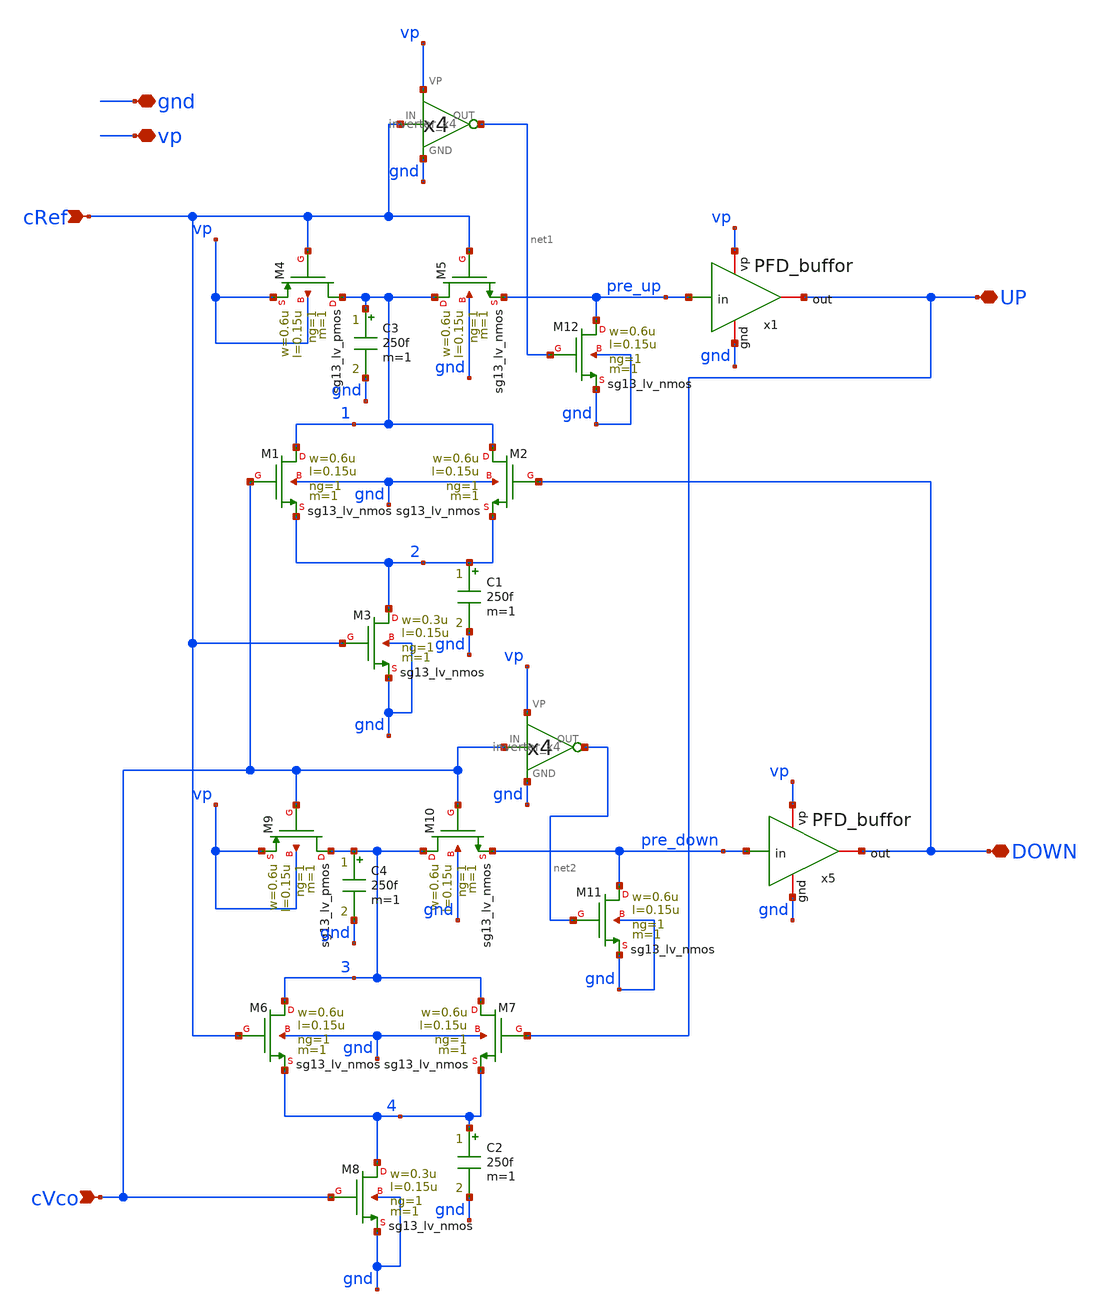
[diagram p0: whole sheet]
** sch_path: PLL0663-main/schematic/xschem/PFD/PFD_cell.sch
**.subckt PFD_cell gnd vp DOWN UP cRef cVco
*.iopin gnd
*.iopin vp
*.iopin DOWN
*.iopin UP
*.ipin cRef
*.ipin cVco
XM1 1 cVco 2 gnd sg13_lv_nmos w=0.6u l=0.15u ng=1 m=1 mm_ok=1
XM2 1 DOWN 2 gnd sg13_lv_nmos w=0.6u l=0.15u ng=1 m=1 mm_ok=1
XM3 2 cRef gnd gnd sg13_lv_nmos w=0.3u l=0.15u ng=1 m=1 mm_ok=1
XM6 3 cRef 4 gnd sg13_lv_nmos w=0.6u l=0.15u ng=1 m=1 mm_ok=1
XM7 3 UP 4 gnd sg13_lv_nmos w=0.6u l=0.15u ng=1 m=1 mm_ok=1
XM8 4 cVco gnd gnd sg13_lv_nmos w=0.3u l=0.15u ng=1 m=1 mm_ok=1
XM4 1 cRef vp vp sg13_lv_pmos w=0.6u l=0.15u ng=1 m=1 mm_ok=1
XM5 1 cRef pre_up gnd sg13_lv_nmos w=0.6u l=0.15u ng=1 m=1 mm_ok=1
XM9 3 cVco vp vp sg13_lv_pmos w=0.6u l=0.15u ng=1 m=1 mm_ok=1
XM10 3 cVco pre_down gnd sg13_lv_nmos w=0.6u l=0.15u ng=1 m=1 mm_ok=1
C2 4 gnd 250f m=1
C1 2 gnd 250f m=1
XM11 pre_down net2 gnd gnd sg13_lv_nmos w=0.6u l=0.15u ng=1 m=1 mm_ok=1
XM12 pre_up net1 gnd gnd sg13_lv_nmos w=0.6u l=0.15u ng=1 m=1 mm_ok=1
C3 1 gnd 250f m=1
C4 3 gnd 250f m=1
x3 cRef net1 vp gnd inverter_x4
x4 cVco net2 vp gnd inverter_x4
x1 gnd vp UP pre_up PFD_buffor
x5 gnd vp DOWN pre_down PFD_buffor
**.ends
.end
